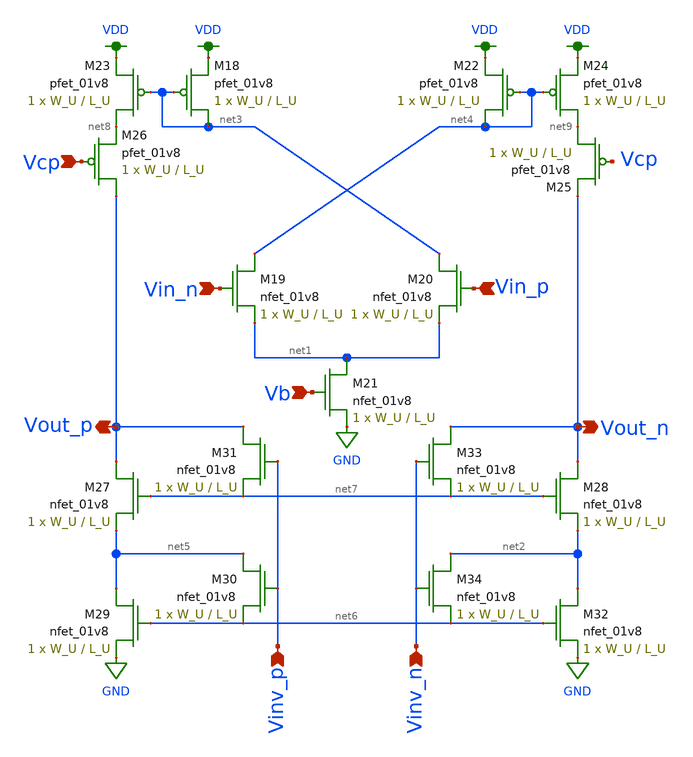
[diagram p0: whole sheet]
** sch_path: schematics/ota.sch
**.subckt ota Vin_n Vin_p Vout_n Vout_p Vcp Vb Vinv_p Vinv_n
*.ipin Vin_n
*.ipin Vin_p
*.opin Vout_n
*.opin Vout_p
*.ipin Vcp
*.ipin Vb
*.ipin Vinv_p
*.ipin Vinv_n
XM18 net3 net3 VDD VDD sky130_fd_pr__pfet_01v8 L=L_U W=W_U nf=1 ad='int((nf+1)/2) * W/nf * 0.29' as='int((nf+2)/2) * W/nf * 0.29'
+ pd='2*int((nf+1)/2) * (W/nf + 0.29)' ps='2*int((nf+2)/2) * (W/nf + 0.29)' nrd='0.29 / W' nrs='0.29 / W'
+ sa=0 sb=0 sd=0 mult=1 m=1
XM19 net4 Vin_n net1 GND sky130_fd_pr__nfet_01v8 L=L_U W=W_U nf=1 ad='int((nf+1)/2) * W/nf * 0.29' as='int((nf+2)/2) * W/nf * 0.29'
+ pd='2*int((nf+1)/2) * (W/nf + 0.29)' ps='2*int((nf+2)/2) * (W/nf + 0.29)' nrd='0.29 / W' nrs='0.29 / W'
+ sa=0 sb=0 sd=0 mult=1 m=1
XM20 net3 Vin_p net1 GND sky130_fd_pr__nfet_01v8 L=L_U W=W_U nf=1 ad='int((nf+1)/2) * W/nf * 0.29' as='int((nf+2)/2) * W/nf * 0.29'
+ pd='2*int((nf+1)/2) * (W/nf + 0.29)' ps='2*int((nf+2)/2) * (W/nf + 0.29)' nrd='0.29 / W' nrs='0.29 / W'
+ sa=0 sb=0 sd=0 mult=1 m=1
XM21 net1 Vb GND GND sky130_fd_pr__nfet_01v8 L=L_U W=W_U nf=1 ad='int((nf+1)/2) * W/nf * 0.29' as='int((nf+2)/2) * W/nf * 0.29'
+ pd='2*int((nf+1)/2) * (W/nf + 0.29)' ps='2*int((nf+2)/2) * (W/nf + 0.29)' nrd='0.29 / W' nrs='0.29 / W'
+ sa=0 sb=0 sd=0 mult=1 m=1
XM22 net4 net4 VDD VDD sky130_fd_pr__pfet_01v8 L=L_U W=W_U nf=1 ad='int((nf+1)/2) * W/nf * 0.29' as='int((nf+2)/2) * W/nf * 0.29'
+ pd='2*int((nf+1)/2) * (W/nf + 0.29)' ps='2*int((nf+2)/2) * (W/nf + 0.29)' nrd='0.29 / W' nrs='0.29 / W'
+ sa=0 sb=0 sd=0 mult=1 m=1
XM23 net8 net3 VDD VDD sky130_fd_pr__pfet_01v8 L=L_U W=W_U nf=1 ad='int((nf+1)/2) * W/nf * 0.29' as='int((nf+2)/2) * W/nf * 0.29'
+ pd='2*int((nf+1)/2) * (W/nf + 0.29)' ps='2*int((nf+2)/2) * (W/nf + 0.29)' nrd='0.29 / W' nrs='0.29 / W'
+ sa=0 sb=0 sd=0 mult=1 m=1
XM24 net9 net4 VDD VDD sky130_fd_pr__pfet_01v8 L=L_U W=W_U nf=1 ad='int((nf+1)/2) * W/nf * 0.29' as='int((nf+2)/2) * W/nf * 0.29'
+ pd='2*int((nf+1)/2) * (W/nf + 0.29)' ps='2*int((nf+2)/2) * (W/nf + 0.29)' nrd='0.29 / W' nrs='0.29 / W'
+ sa=0 sb=0 sd=0 mult=1 m=1
XM25 net9 Vcp Vout_n VDD sky130_fd_pr__pfet_01v8 L=L_U W=W_U nf=1 ad='int((nf+1)/2) * W/nf * 0.29' as='int((nf+2)/2) * W/nf * 0.29'
+ pd='2*int((nf+1)/2) * (W/nf + 0.29)' ps='2*int((nf+2)/2) * (W/nf + 0.29)' nrd='0.29 / W' nrs='0.29 / W'
+ sa=0 sb=0 sd=0 mult=1 m=1
XM26 Vout_p Vcp net8 VDD sky130_fd_pr__pfet_01v8 L=L_U W=W_U nf=1 ad='int((nf+1)/2) * W/nf * 0.29' as='int((nf+2)/2) * W/nf * 0.29'
+ pd='2*int((nf+1)/2) * (W/nf + 0.29)' ps='2*int((nf+2)/2) * (W/nf + 0.29)' nrd='0.29 / W' nrs='0.29 / W'
+ sa=0 sb=0 sd=0 mult=1 m=1
XM27 Vout_p net7 net5 GND sky130_fd_pr__nfet_01v8 L=L_U W=W_U nf=1 ad='int((nf+1)/2) * W/nf * 0.29' as='int((nf+2)/2) * W/nf * 0.29'
+ pd='2*int((nf+1)/2) * (W/nf + 0.29)' ps='2*int((nf+2)/2) * (W/nf + 0.29)' nrd='0.29 / W' nrs='0.29 / W'
+ sa=0 sb=0 sd=0 mult=1 m=1
XM28 Vout_n net7 net2 GND sky130_fd_pr__nfet_01v8 L=L_U W=W_U nf=1 ad='int((nf+1)/2) * W/nf * 0.29' as='int((nf+2)/2) * W/nf * 0.29'
+ pd='2*int((nf+1)/2) * (W/nf + 0.29)' ps='2*int((nf+2)/2) * (W/nf + 0.29)' nrd='0.29 / W' nrs='0.29 / W'
+ sa=0 sb=0 sd=0 mult=1 m=1
XM29 net5 net6 GND GND sky130_fd_pr__nfet_01v8 L=L_U W=W_U nf=1 ad='int((nf+1)/2) * W/nf * 0.29' as='int((nf+2)/2) * W/nf * 0.29'
+ pd='2*int((nf+1)/2) * (W/nf + 0.29)' ps='2*int((nf+2)/2) * (W/nf + 0.29)' nrd='0.29 / W' nrs='0.29 / W'
+ sa=0 sb=0 sd=0 mult=1 m=1
XM30 net5 Vinv_p net6 GND sky130_fd_pr__nfet_01v8 L=L_U W=W_U nf=1 ad='int((nf+1)/2) * W/nf * 0.29' as='int((nf+2)/2) * W/nf * 0.29'
+ pd='2*int((nf+1)/2) * (W/nf + 0.29)' ps='2*int((nf+2)/2) * (W/nf + 0.29)' nrd='0.29 / W' nrs='0.29 / W'
+ sa=0 sb=0 sd=0 mult=1 m=1
XM31 Vout_p Vinv_p net7 GND sky130_fd_pr__nfet_01v8 L=L_U W=W_U nf=1 ad='int((nf+1)/2) * W/nf * 0.29'
+ as='int((nf+2)/2) * W/nf * 0.29' pd='2*int((nf+1)/2) * (W/nf + 0.29)' ps='2*int((nf+2)/2) * (W/nf + 0.29)'
+ nrd='0.29 / W' nrs='0.29 / W' sa=0 sb=0 sd=0 mult=1 m=1
XM32 net2 net6 GND GND sky130_fd_pr__nfet_01v8 L=L_U W=W_U nf=1 ad='int((nf+1)/2) * W/nf * 0.29' as='int((nf+2)/2) * W/nf * 0.29'
+ pd='2*int((nf+1)/2) * (W/nf + 0.29)' ps='2*int((nf+2)/2) * (W/nf + 0.29)' nrd='0.29 / W' nrs='0.29 / W'
+ sa=0 sb=0 sd=0 mult=1 m=1
XM33 Vout_n Vinv_n net7 GND sky130_fd_pr__nfet_01v8 L=L_U W=W_U nf=1 ad='int((nf+1)/2) * W/nf * 0.29'
+ as='int((nf+2)/2) * W/nf * 0.29' pd='2*int((nf+1)/2) * (W/nf + 0.29)' ps='2*int((nf+2)/2) * (W/nf + 0.29)'
+ nrd='0.29 / W' nrs='0.29 / W' sa=0 sb=0 sd=0 mult=1 m=1
XM34 net2 Vinv_n net6 GND sky130_fd_pr__nfet_01v8 L=L_U W=W_U nf=1 ad='int((nf+1)/2) * W/nf * 0.29' as='int((nf+2)/2) * W/nf * 0.29'
+ pd='2*int((nf+1)/2) * (W/nf + 0.29)' ps='2*int((nf+2)/2) * (W/nf + 0.29)' nrd='0.29 / W' nrs='0.29 / W'
+ sa=0 sb=0 sd=0 mult=1 m=1
**.ends
.GLOBAL VDD
.GLOBAL GND
.end
